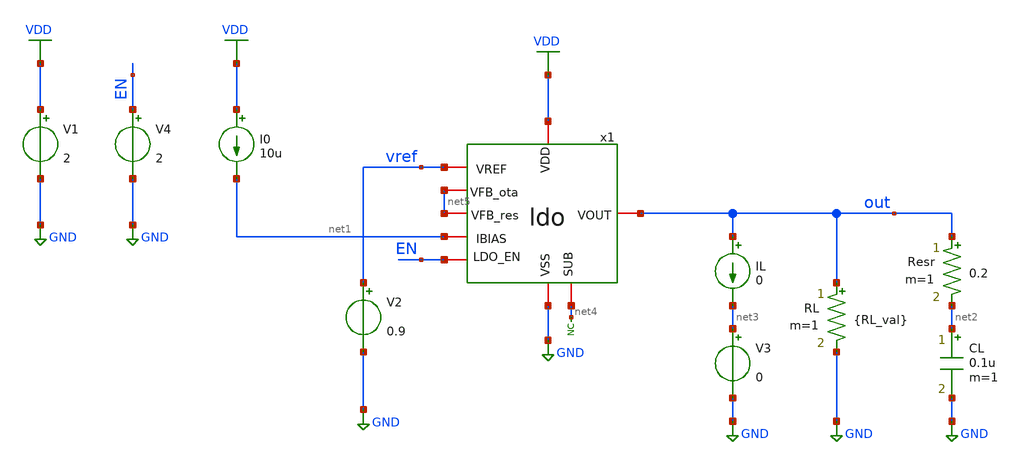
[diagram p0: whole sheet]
** sch_path: designs/libs/tb_ldo/tb_ldo_tran/tb_ldo_tran.sch
**.subckt tb_ldo_tran
RL out GND {RL_val} m=1
V1 VDD GND 2
V2 vref GND 0.9
I0 VDD net1 10u
CL net2 GND 0.1u m=1
Resr out net2 0.2 m=1
IL out net3 0
V3 net3 GND 0
x1 VDD vref out net1 net4 GND EN net5 net5 ldo
* noconn #net4
V4 EN GND 2
**** begin user architecture code



.control
save all

run
set color0 = white

** Define params
.param RL_val = 1.8k

** Define input signal
let fsig = 1k
let tper = 1/fsig
let tfr1 = 10u
let ton1 = 0.5*tper-2*tfr1
let td1 = 10u
let tfr2 = 1u
let ton2 = 0.5*tper-2*tfr2
let td2 = 2u

** Define transient params
let tstop1 = 50u
let tstep1 = 0.01u
let tstop2 = 10u
let tstep2 = 100n

** Transient response to Vdd ramp simulation
alter @V1[PULSE] = [ 2 3.3 $&td1 $&tfr1 $&tfr1 $&ton1 $&tper 0 ]
alter RL = {RL_val}
alter @IL[PULSE] = [ 0 0 $&td1 $&tfr1 $&tfr1 $&ton1 $&tper 0 ]
tran $&tstep1 $&tstop1

** Plots
setplot tran1
let vout = v(out)
let vin = v(vdd)
plot vout
plot vin

write tb_ldo_tran1.raw

** Transient response to Iload ramp simulation
alter @V1[PULSE] = [ 2 2 $&td2 $&tfr2 $&tfr2 $&ton2 $&tper2 0 ]
alter RL = 1e15
alter @IL[PULSE] = [ 0 1m $&td2 $&tfr2 $&tfr2 $&ton2 $&tper 0 ]
tran $&tstep2 $&tstop2

** Plots
setplot tran2
let vout = v(out)
let iload = v3#branch
plot iload
plot vout

write tb_ldo_tran2.raw

** LDO Functional transient simulation
alter @V1[PULSE] = [ 3.3 2 0 1u 1u 248u 500u 0 ]
alter RL = {RL_val}
alter @IL[PULSE] = [ 0 0 0 1u 1u 248u 500u 0 ]
tran 0.5u 500u

** Plots
setplot tran3
let vin = v(vdd)
let vota = v(x1.vota)
let vout = v(out)
plot vin vout vota

write tb_ldo_tran3.raw

** LDO ENABLE SIMULATION
alter @V1[PULSE] = [ 3.3 3.3 0 1u 1u 498u 1m 0 ]
alter RL = {RL_val}
alter @IL[PULSE] = [ 0 0 0 1u 1u 498u 1m 0 ]
alter @V4[PULSE] = [ 0 2 499u 1u 1u 498u 500u 0 ]
tran 0.5u 1m

** Plots
setplot tran4
let vin = v(vdd)
let vout = v(out)
let ENABLE = v(EN)
plot vin vout ENABLE

write tb_ldo_tran4.raw

.endc
* ngspice commands




.include $::180MCU_MODELS/design.ngspice
.lib $::180MCU_MODELS/sm141064.ngspice typical
.lib $::180MCU_MODELS/sm141064.ngspice cap_mim
.lib $::180MCU_MODELS/sm141064.ngspice moscap_typical
.lib $::180MCU_MODELS/sm141064.ngspice mimcap_typical
.lib $::180MCU_MODELS/sm141064.ngspice res_typical
* .lib $::180MCU_MODELS/sm141064.ngspice res_statistical
* ngspice commands

**** end user architecture code
**.ends

* expanding   symbol:  libs/core_ldo/ldo/ldo.sym # of pins=9
** sym_path: designs/libs/core_ldo/ldo/ldo.sym
** sch_path: designs/libs/core_ldo/ldo/ldo.sch
.subckt ldo VDD VREF VOUT IBIAS SUB VSS LDO_EN VFB_ota VFB_res
*.iopin VDD
*.iopin VSS
*.iopin VOUT
*.iopin VREF
*.iopin IBIAS
*.ipin LDO_EN
*.iopin VFB_ota
*.iopin VFB_res
*.iopin SUB
XMpass VOUT Vota VDD VDD pfet_05v0 L=0.50u W=50.00u nf=1 ad='int((nf+1)/2) * W/nf * 0.18u' as='int((nf+2)/2) * W/nf * 0.18u'
+ pd='2*int((nf+1)/2) * (W/nf + 0.18u)' ps='2*int((nf+2)/2) * (W/nf + 0.18u)' nrd='0.18u / W' nrs='0.18u / W'
+ sa=0 sb=0 sd=0 m=10
XR1[9] Vr_fb1[9] VOUT VDD ppolyf_u_1k r_width=1e-6 r_length=5e-6 m=1
XR1[8] Vr_fb1[8] Vr_fb1[9] VDD ppolyf_u_1k r_width=1e-6 r_length=5e-6 m=1
XR1[7] Vr_fb1[7] Vr_fb1[8] VDD ppolyf_u_1k r_width=1e-6 r_length=5e-6 m=1
XR1[6] Vr_fb1[6] Vr_fb1[7] VDD ppolyf_u_1k r_width=1e-6 r_length=5e-6 m=1
XR1[5] Vr_fb1[5] Vr_fb1[6] VDD ppolyf_u_1k r_width=1e-6 r_length=5e-6 m=1
XR1[4] Vr_fb1[4] Vr_fb1[5] VDD ppolyf_u_1k r_width=1e-6 r_length=5e-6 m=1
XR1[3] Vr_fb1[3] Vr_fb1[4] VDD ppolyf_u_1k r_width=1e-6 r_length=5e-6 m=1
XR1[2] Vr_fb1[2] Vr_fb1[3] VDD ppolyf_u_1k r_width=1e-6 r_length=5e-6 m=1
XR1[1] Vr_fb1[1] Vr_fb1[2] VDD ppolyf_u_1k r_width=1e-6 r_length=5e-6 m=1
XR1[0] VFB_res Vr_fb1[1] VDD ppolyf_u_1k r_width=1e-6 r_length=5e-6 m=1
XR2[9] Vr_fb2[9] VFB_res VDD ppolyf_u_1k r_width=1e-6 r_length=5e-6 m=1
XR2[8] Vr_fb2[8] Vr_fb2[9] VDD ppolyf_u_1k r_width=1e-6 r_length=5e-6 m=1
XR2[7] Vr_fb2[7] Vr_fb2[8] VDD ppolyf_u_1k r_width=1e-6 r_length=5e-6 m=1
XR2[6] Vr_fb2[6] Vr_fb2[7] VDD ppolyf_u_1k r_width=1e-6 r_length=5e-6 m=1
XR2[5] Vr_fb2[5] Vr_fb2[6] VDD ppolyf_u_1k r_width=1e-6 r_length=5e-6 m=1
XR2[4] Vr_fb2[4] Vr_fb2[5] VDD ppolyf_u_1k r_width=1e-6 r_length=5e-6 m=1
XR2[3] Vr_fb2[3] Vr_fb2[4] VDD ppolyf_u_1k r_width=1e-6 r_length=5e-6 m=1
XR2[2] Vr_fb2[2] Vr_fb2[3] VDD ppolyf_u_1k r_width=1e-6 r_length=5e-6 m=1
XR2[1] Vr_fb2[1] Vr_fb2[2] VDD ppolyf_u_1k r_width=1e-6 r_length=5e-6 m=1
XR2[0] VSS Vr_fb2[1] VDD ppolyf_u_1k r_width=1e-6 r_length=5e-6 m=1
XRc[29] Vr_mc[29] Vmc VDD ppolyf_u_1k r_width=1e-6 r_length=10e-6 m=1
XRc[28] Vr_mc[28] Vr_mc[29] VDD ppolyf_u_1k r_width=1e-6 r_length=10e-6 m=1
XRc[27] Vr_mc[27] Vr_mc[28] VDD ppolyf_u_1k r_width=1e-6 r_length=10e-6 m=1
XRc[26] Vr_mc[26] Vr_mc[27] VDD ppolyf_u_1k r_width=1e-6 r_length=10e-6 m=1
XRc[25] Vr_mc[25] Vr_mc[26] VDD ppolyf_u_1k r_width=1e-6 r_length=10e-6 m=1
XRc[24] Vr_mc[24] Vr_mc[25] VDD ppolyf_u_1k r_width=1e-6 r_length=10e-6 m=1
XRc[23] Vr_mc[23] Vr_mc[24] VDD ppolyf_u_1k r_width=1e-6 r_length=10e-6 m=1
XRc[22] Vr_mc[22] Vr_mc[23] VDD ppolyf_u_1k r_width=1e-6 r_length=10e-6 m=1
XRc[21] Vr_mc[21] Vr_mc[22] VDD ppolyf_u_1k r_width=1e-6 r_length=10e-6 m=1
XRc[20] Vr_mc[20] Vr_mc[21] VDD ppolyf_u_1k r_width=1e-6 r_length=10e-6 m=1
XRc[19] Vr_mc[19] Vr_mc[20] VDD ppolyf_u_1k r_width=1e-6 r_length=10e-6 m=1
XRc[18] Vr_mc[18] Vr_mc[19] VDD ppolyf_u_1k r_width=1e-6 r_length=10e-6 m=1
XRc[17] Vr_mc[17] Vr_mc[18] VDD ppolyf_u_1k r_width=1e-6 r_length=10e-6 m=1
XRc[16] Vr_mc[16] Vr_mc[17] VDD ppolyf_u_1k r_width=1e-6 r_length=10e-6 m=1
XRc[15] Vr_mc[15] Vr_mc[16] VDD ppolyf_u_1k r_width=1e-6 r_length=10e-6 m=1
XRc[14] Vr_mc[14] Vr_mc[15] VDD ppolyf_u_1k r_width=1e-6 r_length=10e-6 m=1
XRc[13] Vr_mc[13] Vr_mc[14] VDD ppolyf_u_1k r_width=1e-6 r_length=10e-6 m=1
XRc[12] Vr_mc[12] Vr_mc[13] VDD ppolyf_u_1k r_width=1e-6 r_length=10e-6 m=1
XRc[11] Vr_mc[11] Vr_mc[12] VDD ppolyf_u_1k r_width=1e-6 r_length=10e-6 m=1
XRc[10] Vr_mc[10] Vr_mc[11] VDD ppolyf_u_1k r_width=1e-6 r_length=10e-6 m=1
XRc[9] Vr_mc[9] Vr_mc[10] VDD ppolyf_u_1k r_width=1e-6 r_length=10e-6 m=1
XRc[8] Vr_mc[8] Vr_mc[9] VDD ppolyf_u_1k r_width=1e-6 r_length=10e-6 m=1
XRc[7] Vr_mc[7] Vr_mc[8] VDD ppolyf_u_1k r_width=1e-6 r_length=10e-6 m=1
XRc[6] Vr_mc[6] Vr_mc[7] VDD ppolyf_u_1k r_width=1e-6 r_length=10e-6 m=1
XRc[5] Vr_mc[5] Vr_mc[6] VDD ppolyf_u_1k r_width=1e-6 r_length=10e-6 m=1
XRc[4] Vr_mc[4] Vr_mc[5] VDD ppolyf_u_1k r_width=1e-6 r_length=10e-6 m=1
XRc[3] Vr_mc[3] Vr_mc[4] VDD ppolyf_u_1k r_width=1e-6 r_length=10e-6 m=1
XRc[2] Vr_mc[2] Vr_mc[3] VDD ppolyf_u_1k r_width=1e-6 r_length=10e-6 m=1
XRc[1] Vr_mc[1] Vr_mc[2] VDD ppolyf_u_1k r_width=1e-6 r_length=10e-6 m=1
XRc[0] VOUT Vr_mc[1] VDD ppolyf_u_1k r_width=1e-6 r_length=10e-6 m=1
XCc Vota Vmc cap_mim_1f0fF c_width=25e-6 c_length=25e-6 m=4
XRfb_dummy_L[7] VDD VDD VDD ppolyf_u_1k r_width=1e-6 r_length=5e-6 m=1
XRfb_dummy_L[6] VDD VDD VDD ppolyf_u_1k r_width=1e-6 r_length=5e-6 m=1
XRfb_dummy_L[5] VDD VDD VDD ppolyf_u_1k r_width=1e-6 r_length=5e-6 m=1
XRfb_dummy_L[4] VDD VDD VDD ppolyf_u_1k r_width=1e-6 r_length=5e-6 m=1
XRfb_dummy_L[3] VDD VDD VDD ppolyf_u_1k r_width=1e-6 r_length=5e-6 m=1
XRfb_dummy_L[2] VDD VDD VDD ppolyf_u_1k r_width=1e-6 r_length=5e-6 m=1
XRfb_dummy_L[1] VDD VDD VDD ppolyf_u_1k r_width=1e-6 r_length=5e-6 m=1
XRfb_dummy_L[0] VDD VDD VDD ppolyf_u_1k r_width=1e-6 r_length=5e-6 m=1
XRfb_dummy_TB[13] VDD VDD VDD ppolyf_u_1k r_width=1e-6 r_length=5e-6 m=1
XRfb_dummy_TB[12] VDD VDD VDD ppolyf_u_1k r_width=1e-6 r_length=5e-6 m=1
XRfb_dummy_TB[11] VDD VDD VDD ppolyf_u_1k r_width=1e-6 r_length=5e-6 m=1
XRfb_dummy_TB[10] VDD VDD VDD ppolyf_u_1k r_width=1e-6 r_length=5e-6 m=1
XRfb_dummy_TB[9] VDD VDD VDD ppolyf_u_1k r_width=1e-6 r_length=5e-6 m=1
XRfb_dummy_TB[8] VDD VDD VDD ppolyf_u_1k r_width=1e-6 r_length=5e-6 m=1
XRfb_dummy_TB[7] VDD VDD VDD ppolyf_u_1k r_width=1e-6 r_length=5e-6 m=1
XRfb_dummy_TB[6] VDD VDD VDD ppolyf_u_1k r_width=1e-6 r_length=5e-6 m=1
XRfb_dummy_TB[5] VDD VDD VDD ppolyf_u_1k r_width=1e-6 r_length=5e-6 m=1
XRfb_dummy_TB[4] VDD VDD VDD ppolyf_u_1k r_width=1e-6 r_length=5e-6 m=1
XRfb_dummy_TB[3] VDD VDD VDD ppolyf_u_1k r_width=1e-6 r_length=5e-6 m=1
XRfb_dummy_TB[2] VDD VDD VDD ppolyf_u_1k r_width=1e-6 r_length=5e-6 m=1
XRfb_dummy_TB[1] VDD VDD VDD ppolyf_u_1k r_width=1e-6 r_length=5e-6 m=1
XRfb_dummy_TB[0] VDD VDD VDD ppolyf_u_1k r_width=1e-6 r_length=5e-6 m=1
x1 VDD net1 net2 Vota IBIAS VSS OTA
* noconn SUB
x2 VDD LDO_EN ENn VSS biasgen_inverter
x3 VDD ENn ENp VSS biasgen_inverter
XMpenpass Vota ENp VDD VDD pfet_05v0 L=0.5u W=2u nf=1 ad='int((nf+1)/2) * W/nf * 0.18u' as='int((nf+2)/2) * W/nf * 0.18u'
+ pd='2*int((nf+1)/2) * (W/nf + 0.18u)' ps='2*int((nf+2)/2) * (W/nf + 0.18u)' nrd='0.18u / W' nrs='0.18u / W'
+ sa=0 sb=0 sd=0 m=1
.ends


* expanding   symbol:  libs/core_ldo/ldo_OTA/OTA.sym # of pins=6
** sym_path: designs/libs/core_ldo/ldo/OTA.sym
** sch_path: designs/libs/core_ldo/ldo/OTA.sch
.subckt OTA VDD VREF VFB VOTA IBIAS VSS
*.iopin VDD
*.iopin VSS
*.iopin VOTA
*.iopin VREF
*.iopin IBIAS
*.iopin VFB
XM3 net2 net2 VDD VDD pfet_05v0 L=2.00u W=8.00u nf=1 ad='int((nf+1)/2) * W/nf * 0.18u' as='int((nf+2)/2) * W/nf * 0.18u'
+ pd='2*int((nf+1)/2) * (W/nf + 0.18u)' ps='2*int((nf+2)/2) * (W/nf + 0.18u)' nrd='0.18u / W' nrs='0.18u / W'
+ sa=0 sb=0 sd=0 m=1
XM4 net3 net3 VDD VDD pfet_05v0 L=2.00u W=8.00u nf=1 ad='int((nf+1)/2) * W/nf * 0.18u' as='int((nf+2)/2) * W/nf * 0.18u'
+ pd='2*int((nf+1)/2) * (W/nf + 0.18u)' ps='2*int((nf+2)/2) * (W/nf + 0.18u)' nrd='0.18u / W' nrs='0.18u / W'
+ sa=0 sb=0 sd=0 m=1
XM5 net4 net2 VDD VDD pfet_05v0 L=2.00u W=8.00u nf=1 ad='int((nf+1)/2) * W/nf * 0.18u' as='int((nf+2)/2) * W/nf * 0.18u'
+ pd='2*int((nf+1)/2) * (W/nf + 0.18u)' ps='2*int((nf+2)/2) * (W/nf + 0.18u)' nrd='0.18u / W' nrs='0.18u / W'
+ sa=0 sb=0 sd=0 m=1
XM6 VOTA net3 VDD VDD pfet_05v0 L=2.00u W=8.00u nf=1 ad='int((nf+1)/2) * W/nf * 0.18u' as='int((nf+2)/2) * W/nf * 0.18u'
+ pd='2*int((nf+1)/2) * (W/nf + 0.18u)' ps='2*int((nf+2)/2) * (W/nf + 0.18u)' nrd='0.18u / W' nrs='0.18u / W'
+ sa=0 sb=0 sd=0 m=2
XM9 IBIAS IBIAS VSS VSS nfet_05v0 L=2.00u W=4.00u nf=1 ad='int((nf+1)/2) * W/nf * 0.18u' as='int((nf+2)/2) * W/nf * 0.18u'
+ pd='2*int((nf+1)/2) * (W/nf + 0.18u)' ps='2*int((nf+2)/2) * (W/nf + 0.18u)' nrd='0.18u / W' nrs='0.18u / W'
+ sa=0 sb=0 sd=0 m=1
XM10 net1 IBIAS VSS VSS nfet_05v0 L=2.00u W=4.00u nf=1 ad='int((nf+1)/2) * W/nf * 0.18u' as='int((nf+2)/2) * W/nf * 0.18u'
+ pd='2*int((nf+1)/2) * (W/nf + 0.18u)' ps='2*int((nf+2)/2) * (W/nf + 0.18u)' nrd='0.18u / W' nrs='0.18u / W'
+ sa=0 sb=0 sd=0 m=1
XM7 net4 net4 VSS VSS nfet_05v0 L=2.00u W=4.00u nf=1 ad='int((nf+1)/2) * W/nf * 0.18u' as='int((nf+2)/2) * W/nf * 0.18u'
+ pd='2*int((nf+1)/2) * (W/nf + 0.18u)' ps='2*int((nf+2)/2) * (W/nf + 0.18u)' nrd='0.18u / W' nrs='0.18u / W'
+ sa=0 sb=0 sd=0 m=1
XM8 VOTA net4 VSS VSS nfet_05v0 L=2.00u W=4.00u nf=1 ad='int((nf+1)/2) * W/nf * 0.18u' as='int((nf+2)/2) * W/nf * 0.18u'
+ pd='2*int((nf+1)/2) * (W/nf + 0.18u)' ps='2*int((nf+2)/2) * (W/nf + 0.18u)' nrd='0.18u / W' nrs='0.18u / W'
+ sa=0 sb=0 sd=0 m=2
XM1 net2 VREF net1 net1 nfet_05v0 L=0.60u W=40.00u nf=1 ad='int((nf+1)/2) * W/nf * 0.18u' as='int((nf+2)/2) * W/nf * 0.18u'
+ pd='2*int((nf+1)/2) * (W/nf + 0.18u)' ps='2*int((nf+2)/2) * (W/nf + 0.18u)' nrd='0.18u / W' nrs='0.18u / W'
+ sa=0 sb=0 sd=0 m=1
XM2 net3 VFB net1 net1 nfet_05v0 L=0.60u W=40.00u nf=1 ad='int((nf+1)/2) * W/nf * 0.18u' as='int((nf+2)/2) * W/nf * 0.18u'
+ pd='2*int((nf+1)/2) * (W/nf + 0.18u)' ps='2*int((nf+2)/2) * (W/nf + 0.18u)' nrd='0.18u / W' nrs='0.18u / W'
+ sa=0 sb=0 sd=0 m=1
.ends


* expanding   symbol:  libs/core_biasgen/biasgen_inverter/biasgen_inverter.sym # of pins=4
** sym_path: designs/libs/core_biasgen/biasgen_inverter/biasgen_inverter.sym
** sch_path: designs/libs/core_biasgen/biasgen_inverter/biasgen_inverter.sch
.subckt biasgen_inverter VDD IN OUT VSS
*.iopin VDD
*.iopin VSS
*.ipin IN
*.opin OUT
XMINV1 OUT IN VSS VSS nfet_05v0 L=0.60u W=0.50u nf=1 ad='int((nf+1)/2) * W/nf * 0.18u' as='int((nf+2)/2) * W/nf * 0.18u'
+ pd='2*int((nf+1)/2) * (W/nf + 0.18u)' ps='2*int((nf+2)/2) * (W/nf + 0.18u)' nrd='0.18u / W' nrs='0.18u / W'
+ sa=0 sb=0 sd=0 m=1
XMINV2 OUT IN VDD VDD pfet_05v0 L=0.50u W=0.60u nf=1 ad='int((nf+1)/2) * W/nf * 0.18u' as='int((nf+2)/2) * W/nf * 0.18u'
+ pd='2*int((nf+1)/2) * (W/nf + 0.18u)' ps='2*int((nf+2)/2) * (W/nf + 0.18u)' nrd='0.18u / W' nrs='0.18u / W'
+ sa=0 sb=0 sd=0 m=1
.ends

.GLOBAL GND
.GLOBAL VDD
.end
